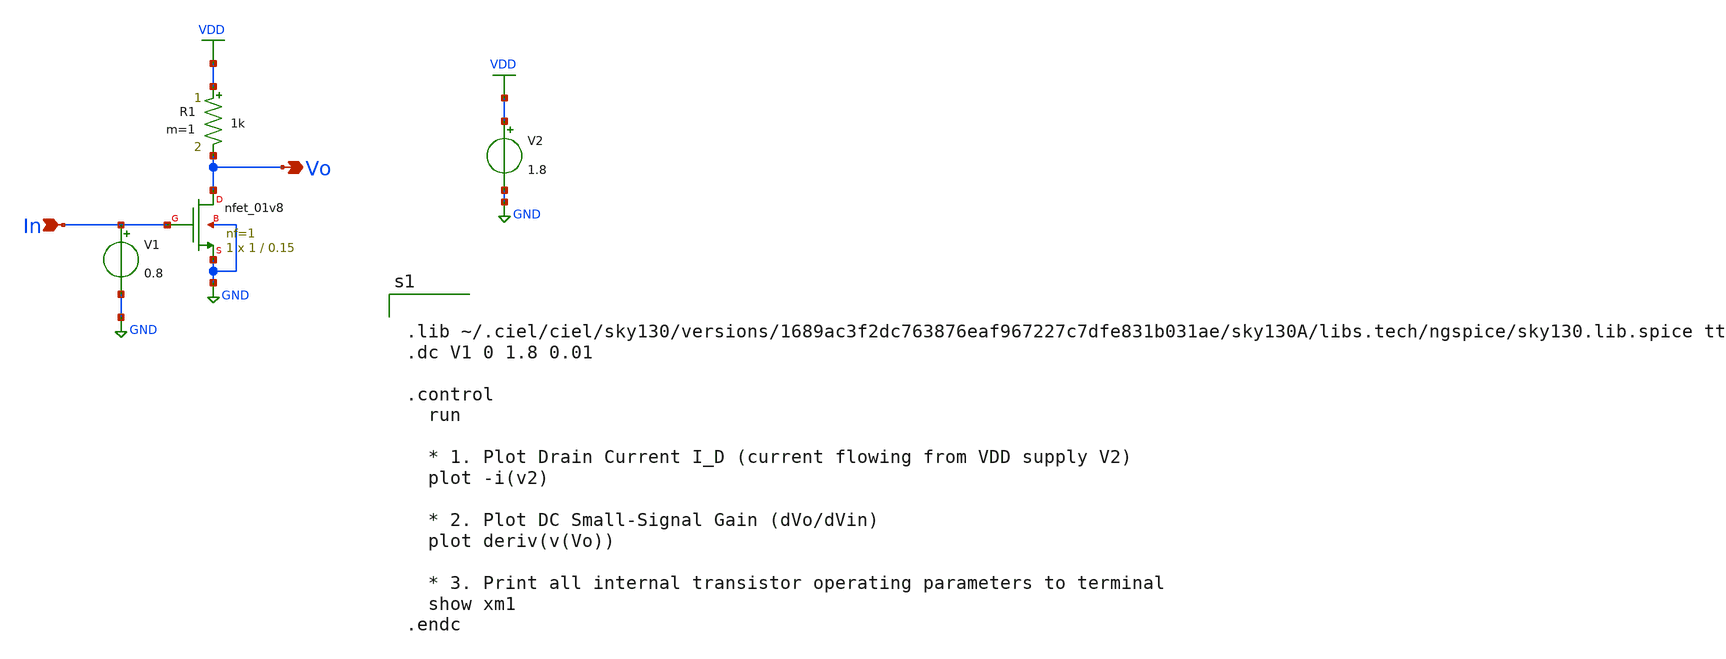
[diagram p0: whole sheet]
** sch_path: SINGLE_STAGE_AMP/CS_RES/cs_res.sch
**.subckt cs_res Vo In
*.opin Vo
*.ipin In
R1 VDD Vo 1k m=1
V1 In GND 0.8
V2 VDD GND 1.8
X}M1 Vo In GND GND sky130_fd_pr__nfet_01v8 L=0.15 W=1 nf=1 ad='int((nf+1)/2) * W/nf * 0.29' as='int((nf+2)/2)
+ * W/nf * 0.29' pd='2*int((nf+1)/2) * (W/nf + 0.29)' ps='2*int((nf+2)/2) * (W/nf + 0.29)' nrd='0.29 /
+ W' nrs='0.29 / W' sa=0 sb=0 sd=0 mult=1 m=1
**** begin user architecture code


.lib ~/.ciel/ciel/sky130/versions/1689ac3f2dc763876eaf967227c7dfe831b031ae/sky130A/libs.tech/ngspice/sky130.lib.spice tt
.dc V1 0 1.8 0.01

.control
  run

  * 1. Plot Drain Current I_D (current flowing from VDD supply V2)
  plot -i(v2)

  * 2. Plot DC Small-Signal Gain (dVo/dVin)
  plot deriv(v(Vo))

  * 3. Print all internal transistor operating parameters to terminal
  show xm1
.endc


**** end user architecture code
**.ends
.GLOBAL VDD
.GLOBAL GND
.end
